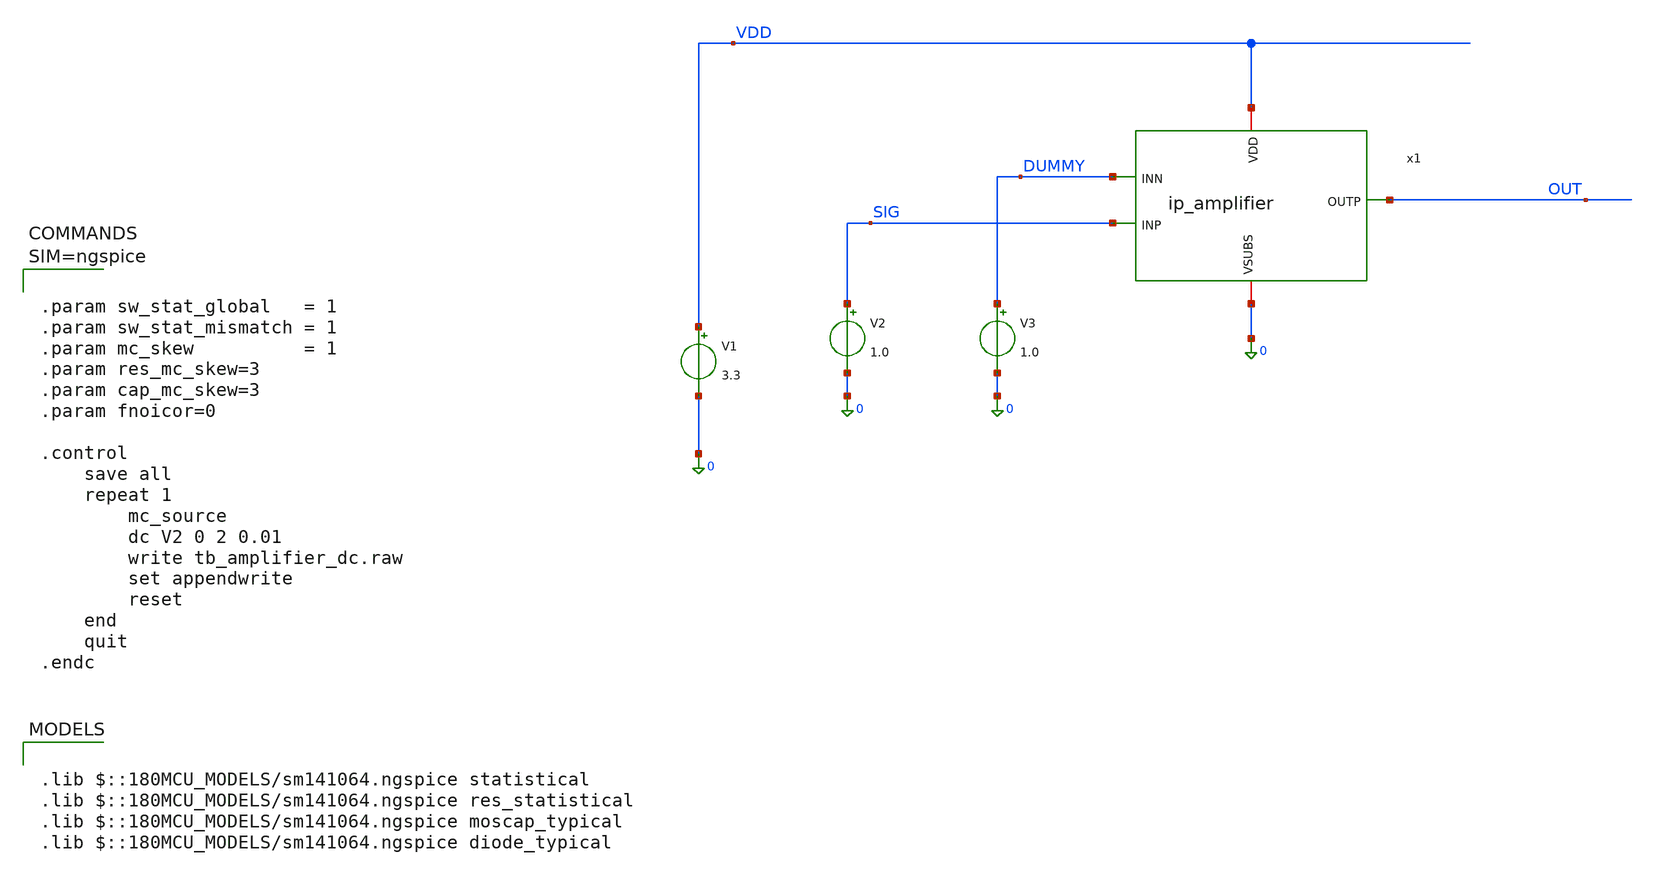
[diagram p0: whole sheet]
** sch_path: xschem/tb_amplifier_dc.sch
**.subckt tb_amplifier_dc
V1 VDD 0 3.3
x1 VDD OUT SIG DUMMY 0 ip_amplifier
V3 DUMMY 0 1.0
V2 SIG 0 1.0
**** begin user architecture code

.lib $::180MCU_MODELS/sm141064.ngspice statistical
.lib $::180MCU_MODELS/sm141064.ngspice res_statistical
.lib $::180MCU_MODELS/sm141064.ngspice moscap_typical
.lib $::180MCU_MODELS/sm141064.ngspice diode_typical




.param sw_stat_global   = 1
.param sw_stat_mismatch = 1
.param mc_skew          = 1
.param res_mc_skew=3
.param cap_mc_skew=3
.param fnoicor=0

.control
	save all
	repeat 1
		mc_source
		dc V2 0 2 0.01
		write tb_amplifier_dc.raw
		set appendwrite
		reset
	end
	quit
.endc



**** end user architecture code
**.ends

* expanding   symbol:  ip_amplifier.sym # of pins=5
** sym_path: xschem/ip_amplifier.sym
** sch_path: xschem/ip_amplifier.sch
.subckt ip_amplifier VDD OUTP INP INN VSUBS
*.iopin VDD
*.iopin VSUBS
*.ipin INP
*.ipin INN
*.opin OUTP
XM1 net9 INP net14 VDD pfet_06v0 L=3u W=20u nf=1 ad='int((nf+1)/2) * W/nf * 0.18u' as='int((nf+2)/2) * W/nf * 0.18u'
+ pd='2*int((nf+1)/2) * (W/nf + 0.18u)' ps='2*int((nf+2)/2) * (W/nf + 0.18u)' nrd='0.18u / W' nrs='0.18u / W'
+ sa=0 sb=0 sd=0 m=10 par=10
XM2 net8 INN net14 VDD pfet_06v0 L=3u W=20u nf=1 ad='int((nf+1)/2) * W/nf * 0.18u' as='int((nf+2)/2) * W/nf * 0.18u'
+ pd='2*int((nf+1)/2) * (W/nf + 0.18u)' ps='2*int((nf+2)/2) * (W/nf + 0.18u)' nrd='0.18u / W' nrs='0.18u / W'
+ sa=0 sb=0 sd=0 m=10 par=10
XM5 net9 net1 VSUBS vsubs nfet_06v0 L=5u W=5u nf=1 ad='int((nf+1)/2) * W/nf * 0.18u' as='int((nf+2)/2) * W/nf * 0.18u'
+ pd='2*int((nf+1)/2) * (W/nf + 0.18u)' ps='2*int((nf+2)/2) * (W/nf + 0.18u)' nrd='0.18u / W' nrs='0.18u / W'
+ sa=0 sb=0 sd=0 m=1 par=1
XM6 net8 net1 VSUBS vsubs nfet_06v0 L=5u W=5u nf=1 ad='int((nf+1)/2) * W/nf * 0.18u' as='int((nf+2)/2) * W/nf * 0.18u'
+ pd='2*int((nf+1)/2) * (W/nf + 0.18u)' ps='2*int((nf+2)/2) * (W/nf + 0.18u)' nrd='0.18u / W' nrs='0.18u / W'
+ sa=0 sb=0 sd=0 m=1 par=1
XM3 net3 net1 VSUBS vsubs nfet_06v0 L=5u W=5u nf=1 ad='int((nf+1)/2) * W/nf * 0.18u' as='int((nf+2)/2) * W/nf * 0.18u'
+ pd='2*int((nf+1)/2) * (W/nf + 0.18u)' ps='2*int((nf+2)/2) * (W/nf + 0.18u)' nrd='0.18u / W' nrs='0.18u / W'
+ sa=0 sb=0 sd=0 m=1 par=1
XM4 net2 net1 VSUBS vsubs nfet_06v0 L=5u W=5u nf=1 ad='int((nf+1)/2) * W/nf * 0.18u' as='int((nf+2)/2) * W/nf * 0.18u'
+ pd='2*int((nf+1)/2) * (W/nf + 0.18u)' ps='2*int((nf+2)/2) * (W/nf + 0.18u)' nrd='0.18u / W' nrs='0.18u / W'
+ sa=0 sb=0 sd=0 m=1 par=1
XM7 net1 net1 net3 vsubs nfet_06v0 L=2u W=10u nf=1 ad='int((nf+1)/2) * W/nf * 0.18u' as='int((nf+2)/2) * W/nf * 0.18u'
+ pd='2*int((nf+1)/2) * (W/nf + 0.18u)' ps='2*int((nf+2)/2) * (W/nf + 0.18u)' nrd='0.18u / W' nrs='0.18u / W'
+ sa=0 sb=0 sd=0 m=1 par=1
XM8 net4 net1 net2 vsubs nfet_06v0 L=2u W=10u nf=1 ad='int((nf+1)/2) * W/nf * 0.18u' as='int((nf+2)/2) * W/nf * 0.18u'
+ pd='2*int((nf+1)/2) * (W/nf + 0.18u)' ps='2*int((nf+2)/2) * (W/nf + 0.18u)' nrd='0.18u / W' nrs='0.18u / W'
+ sa=0 sb=0 sd=0 m=1 par=1
I0 VDD net1 5u
XM9 net5 net4 VDD VDD pfet_06v0 L=5u W=15u nf=1 ad='int((nf+1)/2) * W/nf * 0.18u' as='int((nf+2)/2) * W/nf * 0.18u'
+ pd='2*int((nf+1)/2) * (W/nf + 0.18u)' ps='2*int((nf+2)/2) * (W/nf + 0.18u)' nrd='0.18u / W' nrs='0.18u / W'
+ sa=0 sb=0 sd=0 m=1 par=1
XM10 net6 net4 VDD VDD pfet_06v0 L=5u W=15u nf=1 ad='int((nf+1)/2) * W/nf * 0.18u' as='int((nf+2)/2) * W/nf * 0.18u'
+ pd='2*int((nf+1)/2) * (W/nf + 0.18u)' ps='2*int((nf+2)/2) * (W/nf + 0.18u)' nrd='0.18u / W' nrs='0.18u / W'
+ sa=0 sb=0 sd=0 m=2 par=2
XM11 net4 net4 net5 VDD pfet_06v0 L=2u W=20u nf=1 ad='int((nf+1)/2) * W/nf * 0.18u' as='int((nf+2)/2) * W/nf * 0.18u'
+ pd='2*int((nf+1)/2) * (W/nf + 0.18u)' ps='2*int((nf+2)/2) * (W/nf + 0.18u)' nrd='0.18u / W' nrs='0.18u / W'
+ sa=0 sb=0 sd=0 m=1 par=1
XM12 net7 net4 net6 VDD pfet_06v0 L=2u W=20u nf=1 ad='int((nf+1)/2) * W/nf * 0.18u' as='int((nf+2)/2) * W/nf * 0.18u'
+ pd='2*int((nf+1)/2) * (W/nf + 0.18u)' ps='2*int((nf+2)/2) * (W/nf + 0.18u)' nrd='0.18u / W' nrs='0.18u / W'
+ sa=0 sb=0 sd=0 m=2 par=2
XM13 net13 net1 net8 vsubs nfet_06v0 L=10u W=5u nf=1 ad='int((nf+1)/2) * W/nf * 0.18u' as='int((nf+2)/2) * W/nf * 0.18u'
+ pd='2*int((nf+1)/2) * (W/nf + 0.18u)' ps='2*int((nf+2)/2) * (W/nf + 0.18u)' nrd='0.18u / W' nrs='0.18u / W'
+ sa=0 sb=0 sd=0 m=1 par=1
XM14 OUTP net1 net9 vsubs nfet_06v0 L=10u W=5u nf=1 ad='int((nf+1)/2) * W/nf * 0.18u' as='int((nf+2)/2) * W/nf * 0.18u'
+ pd='2*int((nf+1)/2) * (W/nf + 0.18u)' ps='2*int((nf+2)/2) * (W/nf + 0.18u)' nrd='0.18u / W' nrs='0.18u / W'
+ sa=0 sb=0 sd=0 m=1 par=1
XM15 net10 net12 VDD VDD pfet_06v0 L=5u W=20u nf=1 ad='int((nf+1)/2) * W/nf * 0.18u' as='int((nf+2)/2) * W/nf * 0.18u'
+ pd='2*int((nf+1)/2) * (W/nf + 0.18u)' ps='2*int((nf+2)/2) * (W/nf + 0.18u)' nrd='0.18u / W' nrs='0.18u / W'
+ sa=0 sb=0 sd=0 m=2 par=2
XM16 net11 net12 VDD VDD pfet_06v0 L=5u W=20u nf=1 ad='int((nf+1)/2) * W/nf * 0.18u' as='int((nf+2)/2) * W/nf * 0.18u'
+ pd='2*int((nf+1)/2) * (W/nf + 0.18u)' ps='2*int((nf+2)/2) * (W/nf + 0.18u)' nrd='0.18u / W' nrs='0.18u / W'
+ sa=0 sb=0 sd=0 m=2 par=2
XM17 net16 net15 net11 VDD pfet_06v0 L=2u W=20u nf=1 ad='int((nf+1)/2) * W/nf * 0.18u' as='int((nf+2)/2) * W/nf * 0.18u'
+ pd='2*int((nf+1)/2) * (W/nf + 0.18u)' ps='2*int((nf+2)/2) * (W/nf + 0.18u)' nrd='0.18u / W' nrs='0.18u / W'
+ sa=0 sb=0 sd=0 m=5 par=5
XM18 net12 net15 net10 VDD pfet_06v0 L=2u W=20u nf=1 ad='int((nf+1)/2) * W/nf * 0.18u' as='int((nf+2)/2) * W/nf * 0.18u'
+ pd='2*int((nf+1)/2) * (W/nf + 0.18u)' ps='2*int((nf+2)/2) * (W/nf + 0.18u)' nrd='0.18u / W' nrs='0.18u / W'
+ sa=0 sb=0 sd=0 m=5 par=5
Vmeas net7 net14 0
Vmeas1 net15 net13 0
Vmeas2 net16 OUTP 0
R1 net12 net15 50k m=1
.ends

.end
